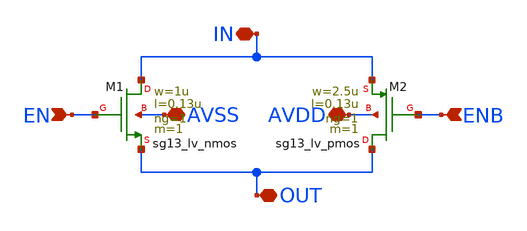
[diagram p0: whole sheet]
** sch_path: designs/libs/core_digital/tgate/tgate.sch
**.subckt tgate AVDD AVSS IN OUT EN ENB
*.iopin AVDD
*.iopin AVSS
*.iopin IN
*.iopin OUT
*.ipin EN
*.ipin ENB
XM1 IN EN OUT AVSS sg13_lv_nmos w=1u l=0.13u ng=1 m=1 mm_ok=1
XM2 OUT ENB IN AVDD sg13_lv_pmos w=2.5u l=0.13u ng=1 m=1 mm_ok=1
**.ends
.end
